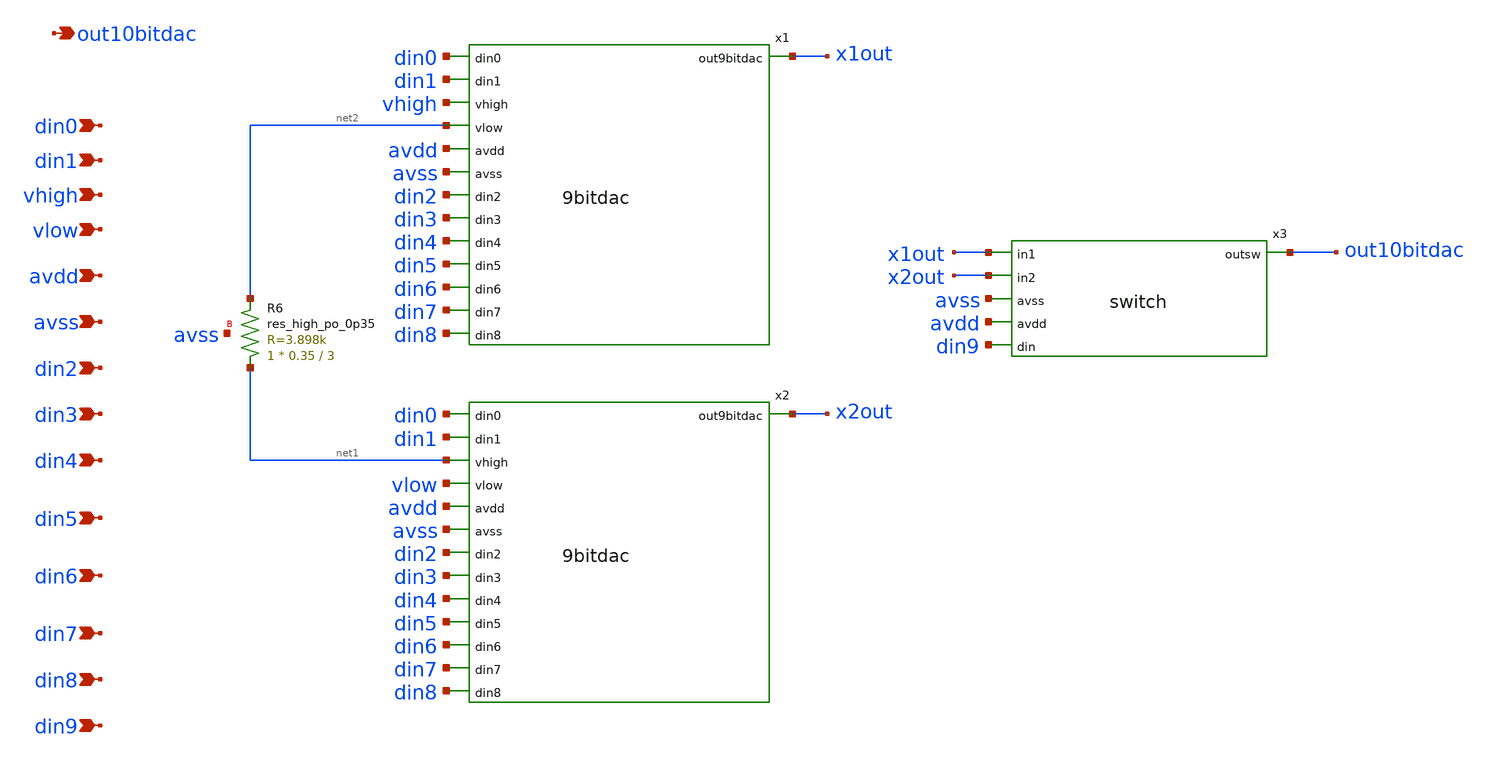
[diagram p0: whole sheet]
** sch_path: xschem/10bitdac.sch
**.subckt 10bitdac din0 din1 vhigh vlow avdd avss din2 din3 out10bitdac din4 din5 din6 din7 din8
*+ din9
*.ipin din0
*.ipin din1
*.ipin vhigh
*.ipin vlow
*.ipin avdd
*.ipin avss
*.ipin din2
*.ipin din3
*.opin out10bitdac
*.ipin din4
*.ipin din5
*.ipin din6
*.ipin din7
*.ipin din8
*.ipin din9
x1 x1out din0 din1 vhigh net2 avdd avss din2 din3 din4 din5 din6 din7 din8 9bitdac
x2 x2out din0 din1 net1 vlow avdd avss din2 din3 din4 din5 din6 din7 din8 9bitdac
XR6 net1 net2 avss sky130_fd_pr__res_high_po_0p35 L=3 mult=1 m=1
x3 out10bitdac x1out x2out avss avdd din9 switch
**.ends
.end
